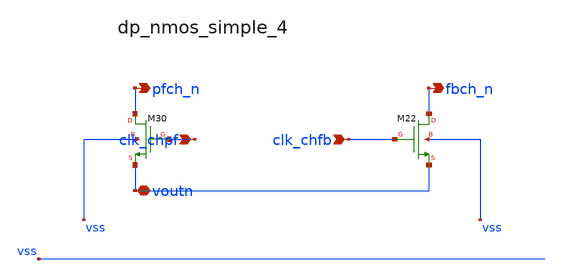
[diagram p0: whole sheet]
** sch_path: analog-db/raw/ia_003_fan_chopper_pf/hier/blocks/dp_nmos_simple_4.sch
**.subckt dp_nmos_simple_4 clk_chpf clk_chfb voutn pfch_n fbch_n
*.ipin clk_chpf
*.ipin clk_chfb
*.iopin voutn
*.opin pfch_n
*.opin fbch_n
XM22 fbch_n clk_chfb voutn vss sg13_lv_nmos w=x_dut_xm22_w l=x_dut_xm22_l ng=1 m=x_dut_xm22_m
XM30 pfch_n clk_chpf voutn vss sg13_lv_nmos w=x_dut_xm30_w l=x_dut_xm30_l ng=1 m=x_dut_xm30_m
**.ends
.end
